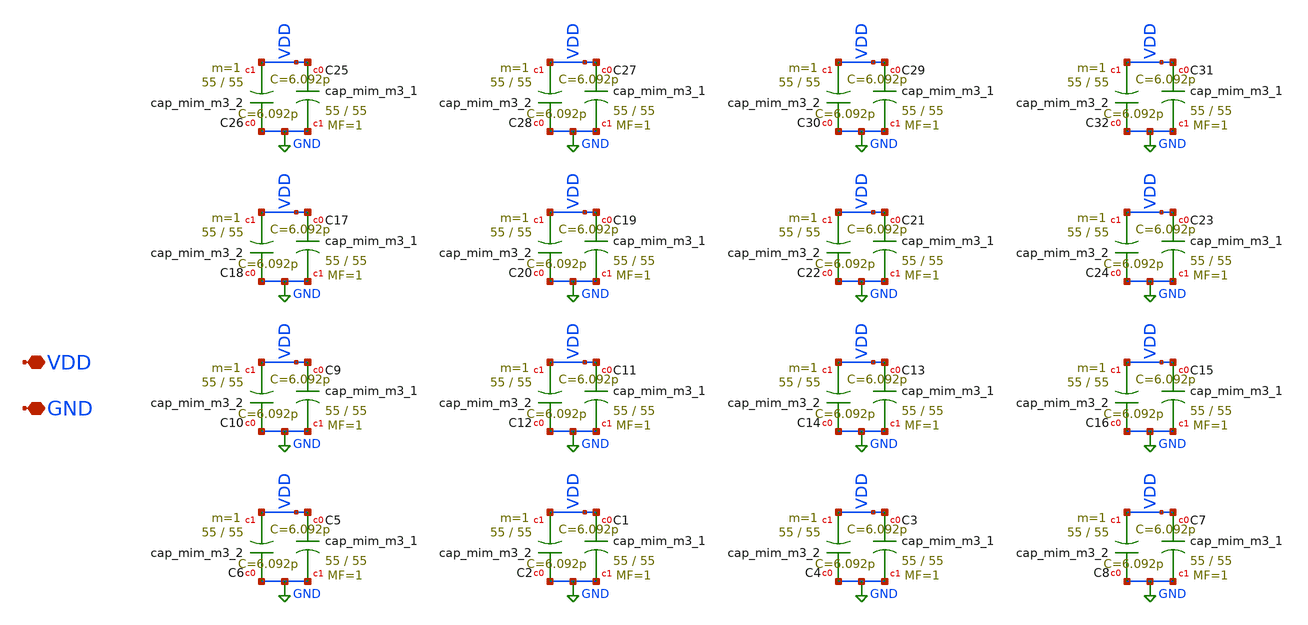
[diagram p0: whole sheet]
** sch_path: xschem/big_cap.sch
**.subckt big_cap VDD GND
*.iopin VDD
*.iopin GND
XC5 VDD GND sky130_fd_pr__cap_mim_m3_1 W=55 L=55 MF=1 m=1
XC6 GND VDD sky130_fd_pr__cap_mim_m3_2 W=55 L=55 MF=1 m=1
XC1 VDD GND sky130_fd_pr__cap_mim_m3_1 W=55 L=55 MF=1 m=1
XC2 GND VDD sky130_fd_pr__cap_mim_m3_2 W=55 L=55 MF=1 m=1
XC3 VDD GND sky130_fd_pr__cap_mim_m3_1 W=55 L=55 MF=1 m=1
XC4 GND VDD sky130_fd_pr__cap_mim_m3_2 W=55 L=55 MF=1 m=1
XC7 VDD GND sky130_fd_pr__cap_mim_m3_1 W=55 L=55 MF=1 m=1
XC8 GND VDD sky130_fd_pr__cap_mim_m3_2 W=55 L=55 MF=1 m=1
XC9 VDD GND sky130_fd_pr__cap_mim_m3_1 W=55 L=55 MF=1 m=1
XC10 GND VDD sky130_fd_pr__cap_mim_m3_2 W=55 L=55 MF=1 m=1
XC11 VDD GND sky130_fd_pr__cap_mim_m3_1 W=55 L=55 MF=1 m=1
XC12 GND VDD sky130_fd_pr__cap_mim_m3_2 W=55 L=55 MF=1 m=1
XC13 VDD GND sky130_fd_pr__cap_mim_m3_1 W=55 L=55 MF=1 m=1
XC14 GND VDD sky130_fd_pr__cap_mim_m3_2 W=55 L=55 MF=1 m=1
XC15 VDD GND sky130_fd_pr__cap_mim_m3_1 W=55 L=55 MF=1 m=1
XC16 GND VDD sky130_fd_pr__cap_mim_m3_2 W=55 L=55 MF=1 m=1
XC17 VDD GND sky130_fd_pr__cap_mim_m3_1 W=55 L=55 MF=1 m=1
XC18 GND VDD sky130_fd_pr__cap_mim_m3_2 W=55 L=55 MF=1 m=1
XC19 VDD GND sky130_fd_pr__cap_mim_m3_1 W=55 L=55 MF=1 m=1
XC20 GND VDD sky130_fd_pr__cap_mim_m3_2 W=55 L=55 MF=1 m=1
XC21 VDD GND sky130_fd_pr__cap_mim_m3_1 W=55 L=55 MF=1 m=1
XC22 GND VDD sky130_fd_pr__cap_mim_m3_2 W=55 L=55 MF=1 m=1
XC23 VDD GND sky130_fd_pr__cap_mim_m3_1 W=55 L=55 MF=1 m=1
XC24 GND VDD sky130_fd_pr__cap_mim_m3_2 W=55 L=55 MF=1 m=1
XC25 VDD GND sky130_fd_pr__cap_mim_m3_1 W=55 L=55 MF=1 m=1
XC26 GND VDD sky130_fd_pr__cap_mim_m3_2 W=55 L=55 MF=1 m=1
XC27 VDD GND sky130_fd_pr__cap_mim_m3_1 W=55 L=55 MF=1 m=1
XC28 GND VDD sky130_fd_pr__cap_mim_m3_2 W=55 L=55 MF=1 m=1
XC29 VDD GND sky130_fd_pr__cap_mim_m3_1 W=55 L=55 MF=1 m=1
XC30 GND VDD sky130_fd_pr__cap_mim_m3_2 W=55 L=55 MF=1 m=1
XC31 VDD GND sky130_fd_pr__cap_mim_m3_1 W=55 L=55 MF=1 m=1
XC32 GND VDD sky130_fd_pr__cap_mim_m3_2 W=55 L=55 MF=1 m=1
**.ends
.GLOBAL GND
.end
